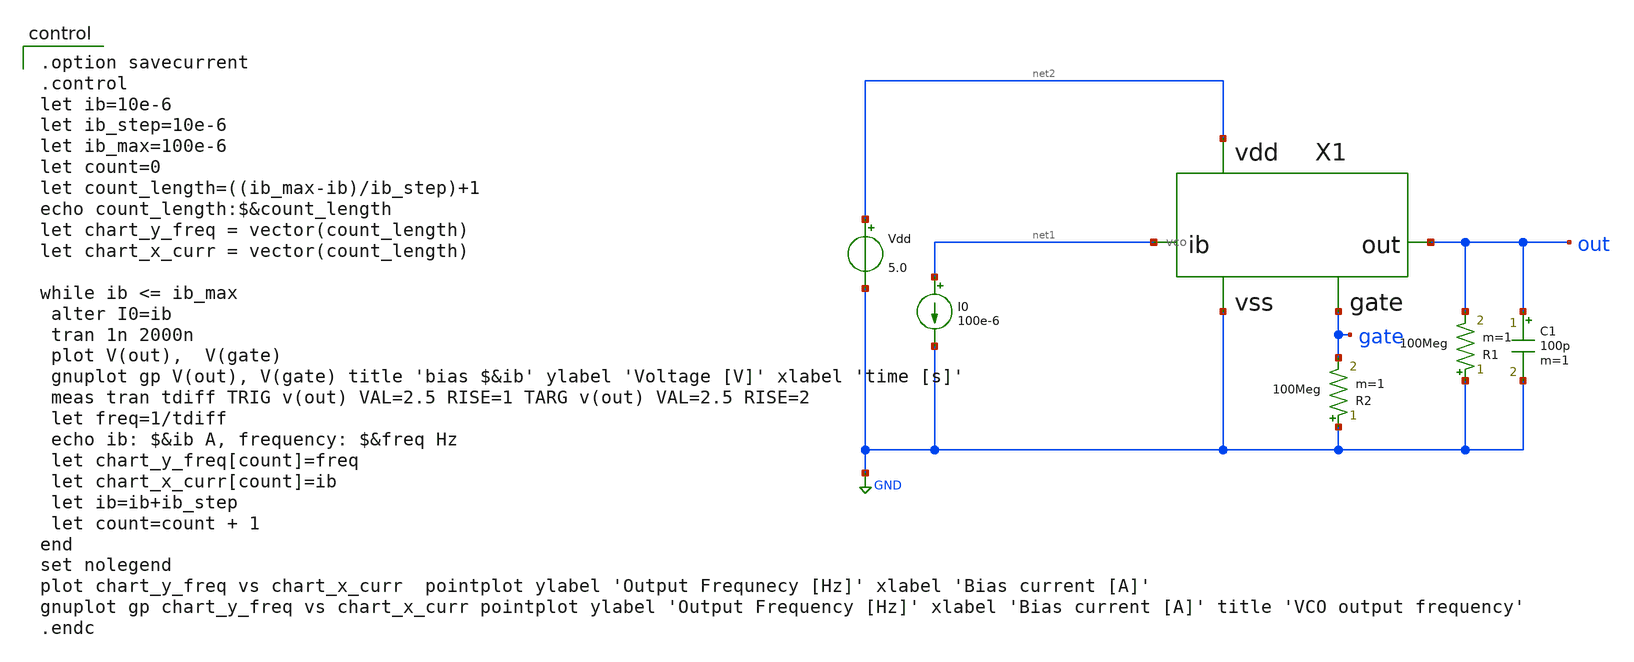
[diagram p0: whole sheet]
** sch_path: IO_202604/10/xschem/vco_testbench.sch
**.subckt vco_testbench
Vdd net2 GND 5.0
C1 out GND 100p m=1
I0 net1 GND 100e-6
R1 GND out 100Meg m=1
X1 net1 out net2 GND gate vco
R2 GND gate 100Meg m=1
**** begin user architecture code

.option savecurrent
.control
let ib=10e-6
let ib_step=10e-6
let ib_max=100e-6
let count=0
let count_length=((ib_max-ib)/ib_step)+1
echo count_length:$&count_length
let chart_y_freq = vector(count_length)
let chart_x_curr = vector(count_length)

while ib <= ib_max
 alter I0=ib
 tran 1n 2000n
 plot V(out),  V(gate)
 gnuplot gp V(out), V(gate) title 'bias $&ib' ylabel 'Voltage [V]' xlabel 'time [s]'
 meas tran tdiff TRIG v(out) VAL=2.5 RISE=1 TARG v(out) VAL=2.5 RISE=2
 let freq=1/tdiff
 echo ib: $&ib A, frequency: $&freq Hz
 let chart_y_freq[count]=freq
 let chart_x_curr[count]=ib
 let ib=ib+ib_step
 let count=count + 1
end
set nolegend
plot chart_y_freq vs chart_x_curr  pointplot ylabel 'Output Frequnecy [Hz]' xlabel 'Bias current [A]'
gnuplot gp chart_y_freq vs chart_x_curr pointplot ylabel 'Output Frequency [Hz]' xlabel 'Bias current [A]'
+ title 'VCO output frequency'
.endc

 .include $::LIB/../ip62_models
**** end user architecture code
**.ends

* expanding   symbol:  vco.sym # of pins=5
** sym_path: Vol.2/files/06/xschem/vco.sym
** sch_path: Vol.2/files/06/xschem/vco.sch
.subckt vco ib out vdd vss gate
*.opin out
*.iopin vdd
*.iopin vss
*.iopin ib
*.iopin gate
XM1 ib ib vdd vdd PMOS w=30u l=2u as=0 ad=0 ps=0 pd=0 nrd=0 nrs=0 m=1
XM3 net3 net4 net1 net1 PMOS w=12u l=2u as=0 ad=0 ps=0 pd=0 nrd=0 nrs=0 m=1
XM6 net3 net4 net2 vss NMOS w=4u l=2u as=0 ad=0 ps=0 pd=0 nrd=0 nrs=0 m=1
XM7 net1 ib vdd vdd PMOS w=30u l=2u as=0 ad=0 ps=0 pd=0 nrd=0 nrs=0 m=1
XM8 gate net3 net1 net1 PMOS w=12u l=2u as=0 ad=0 ps=0 pd=0 nrd=0 nrs=0 m=1
XM9 gate net3 net2 vss NMOS w=4u l=2u as=0 ad=0 ps=0 pd=0 nrd=0 nrs=0 m=1
XM12 net4 gate vdd vdd PMOS w=300u l=1u as=0 ad=0 ps=0 pd=0 nrd=0 nrs=0 m=1
XM13 net4 gate vss vss NMOS w=100u l=1u as=0 ad=0 ps=0 pd=0 nrd=0 nrs=0 m=1
XM2 out net4 vdd vdd PMOS w=600u l=1u as=0 ad=0 ps=0 pd=0 nrd=0 nrs=0 m=1
XM4 out net4 vss vss NMOS w=200u l=1u as=0 ad=0 ps=0 pd=0 nrd=0 nrs=0 m=1
XM5 net5 ib vdd vdd PMOS w=30u l=2u as=0 ad=0 ps=0 pd=0 nrd=0 nrs=0 m=1
XM10 net5 net5 vss vss NMOS w=10u l=2u as=0 ad=0 ps=0 pd=0 nrd=0 nrs=0 m=1
XM11 net2 net5 vss vss NMOS w=10u l=2u as=0 ad=0 ps=0 pd=0 nrd=0 nrs=0 m=1
XC1 gate vss vss F_CSIO c=8.856p x=120u y=120u m=1
.ends

.GLOBAL GND
.end
